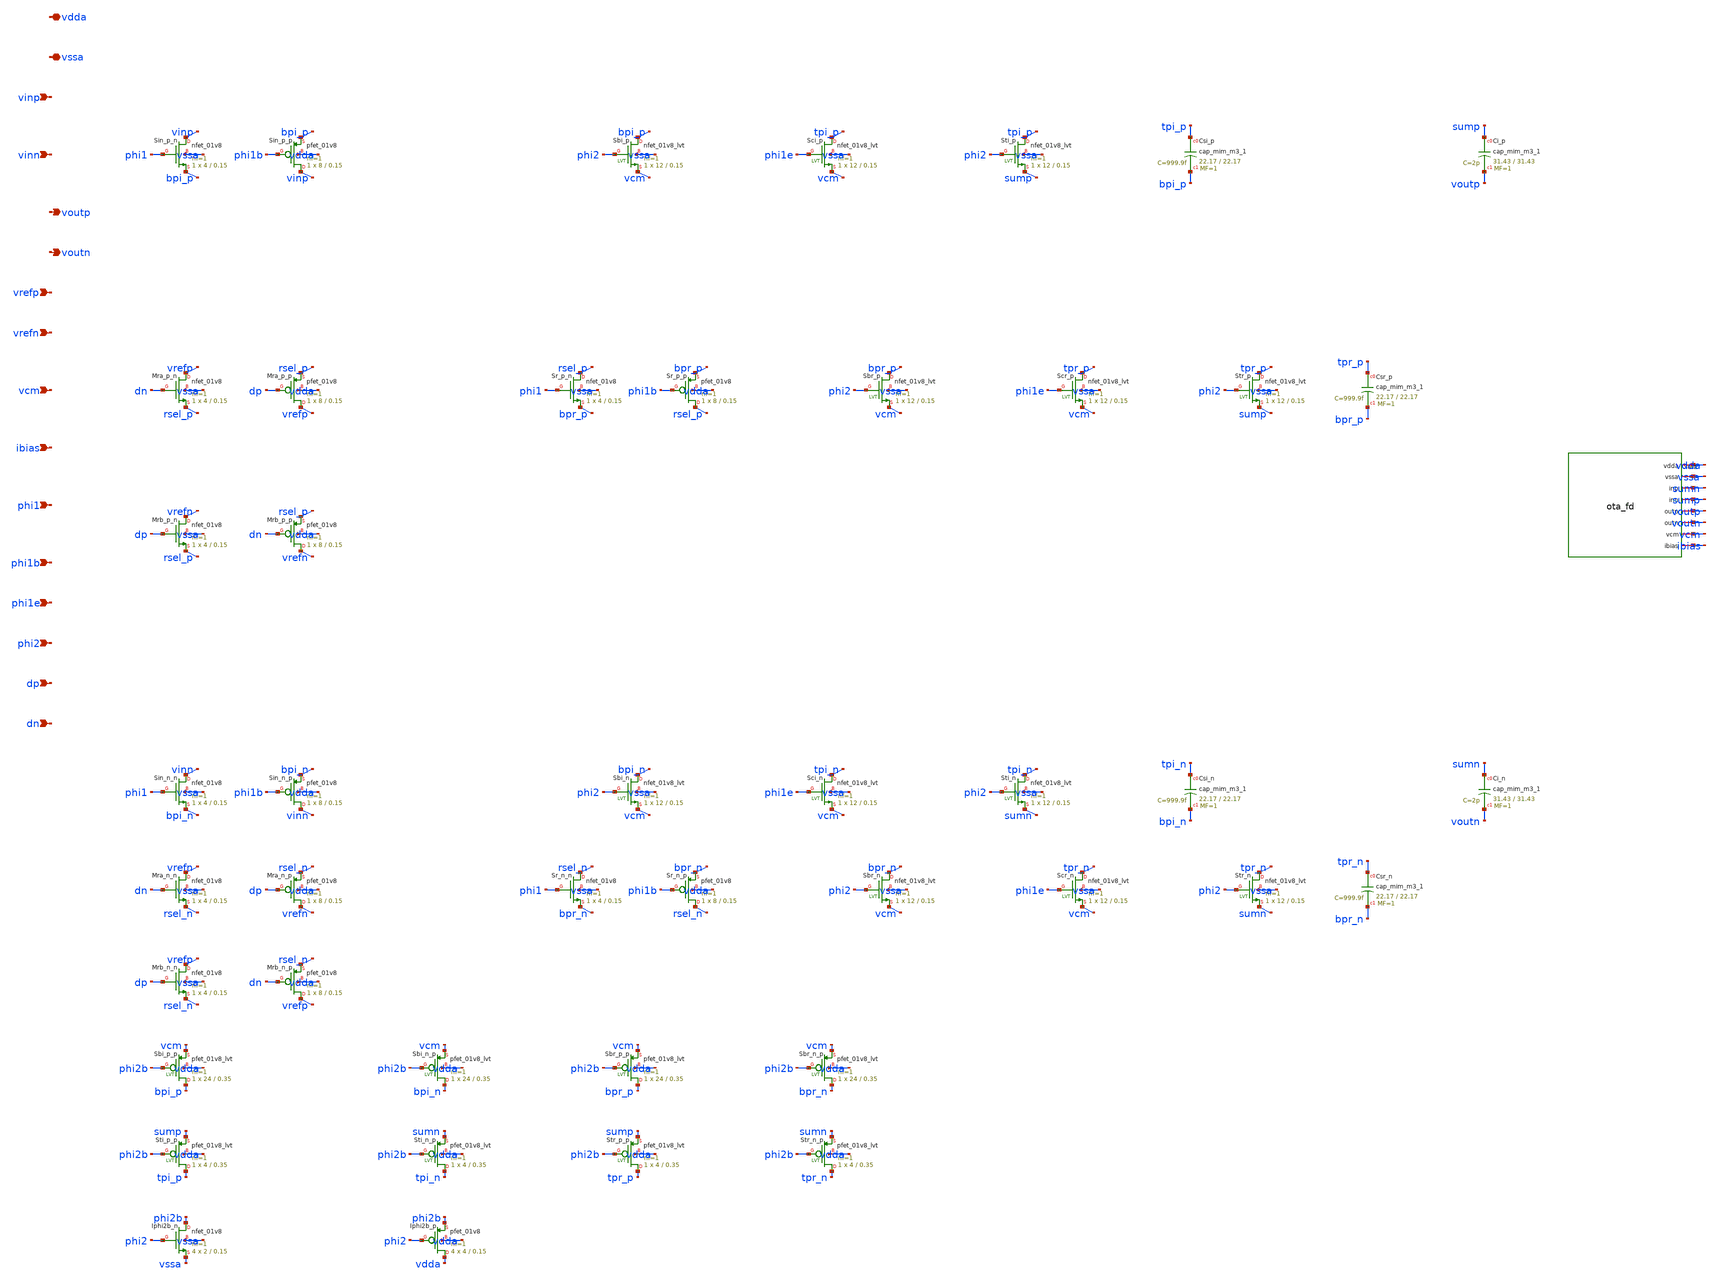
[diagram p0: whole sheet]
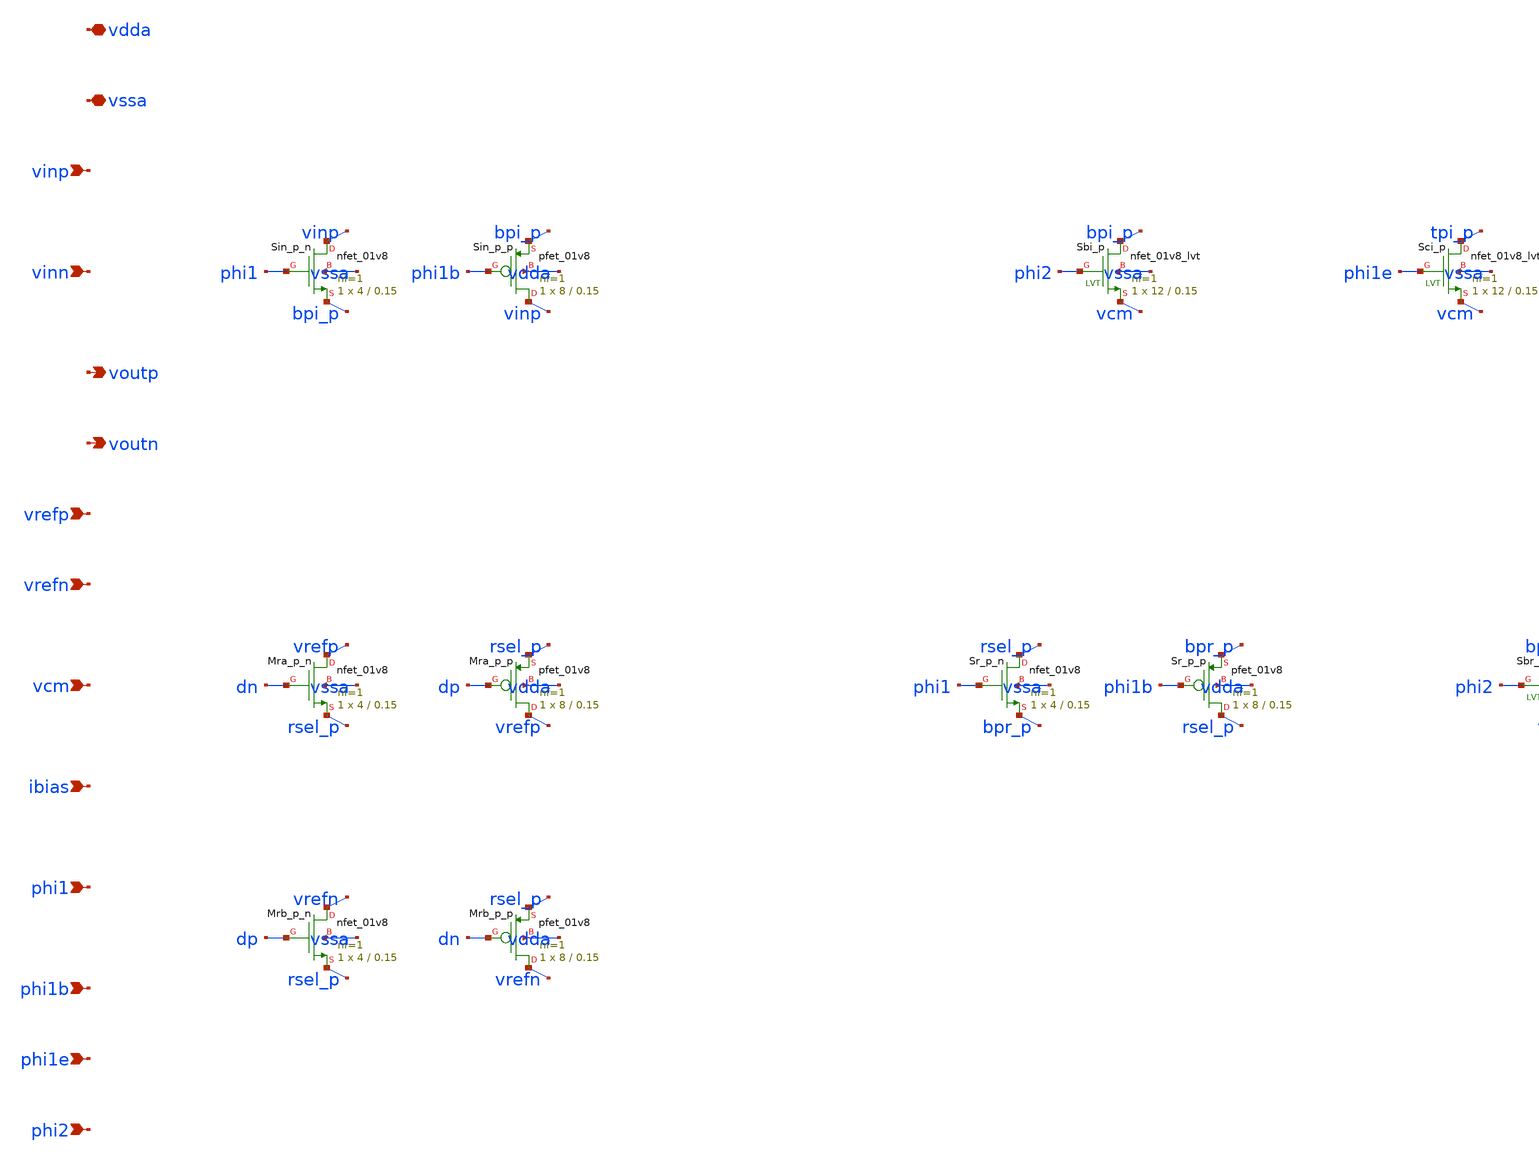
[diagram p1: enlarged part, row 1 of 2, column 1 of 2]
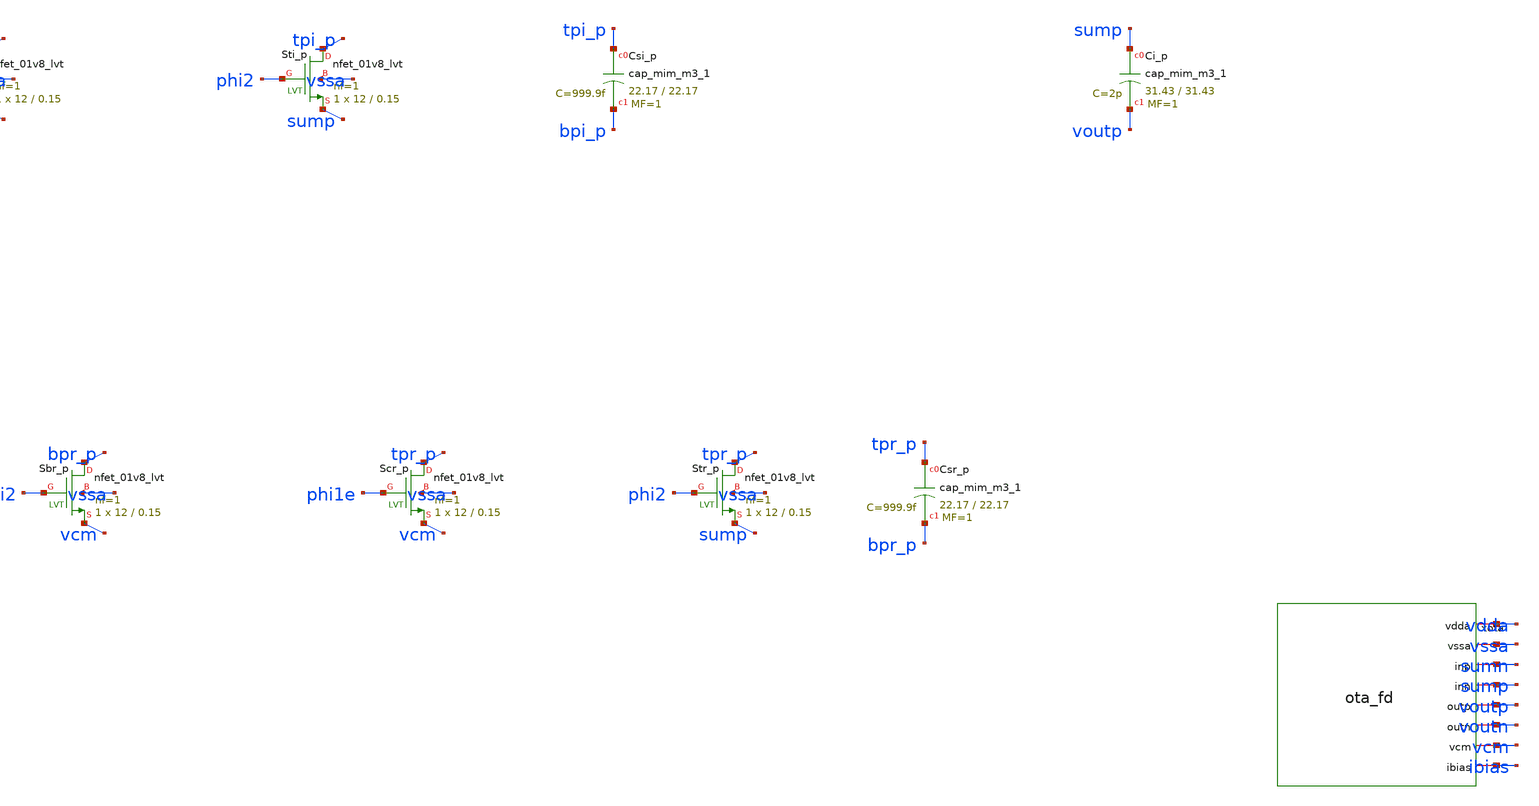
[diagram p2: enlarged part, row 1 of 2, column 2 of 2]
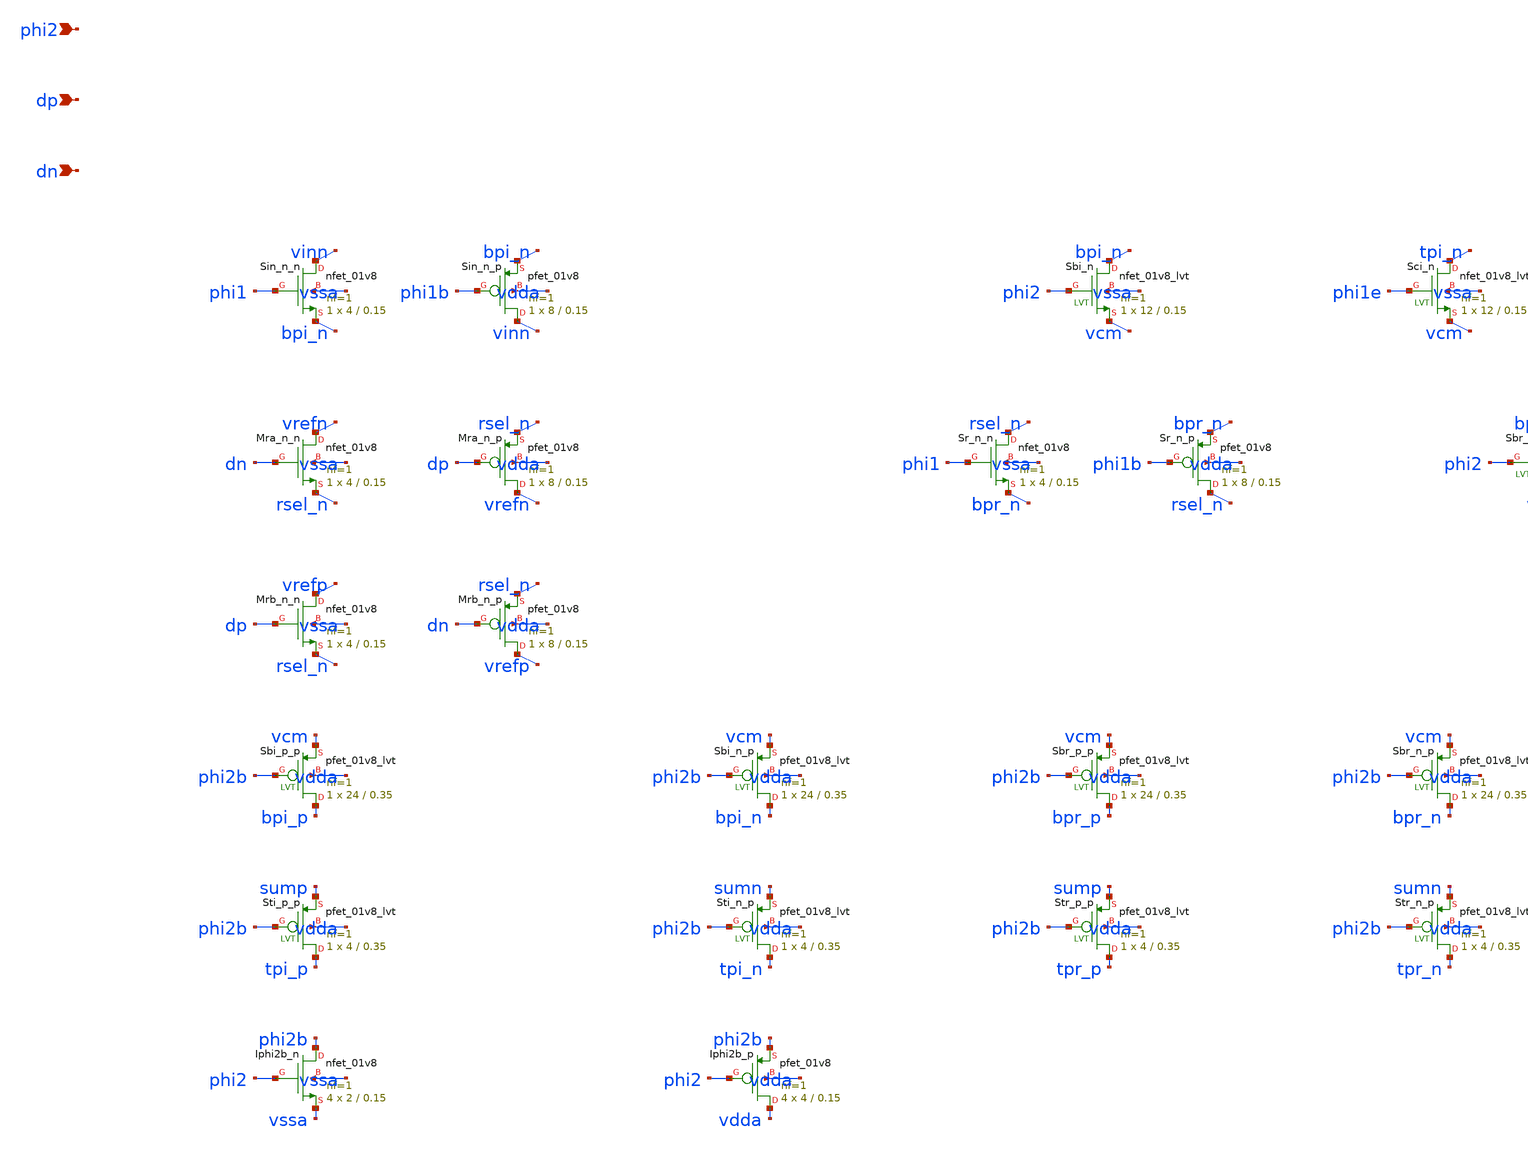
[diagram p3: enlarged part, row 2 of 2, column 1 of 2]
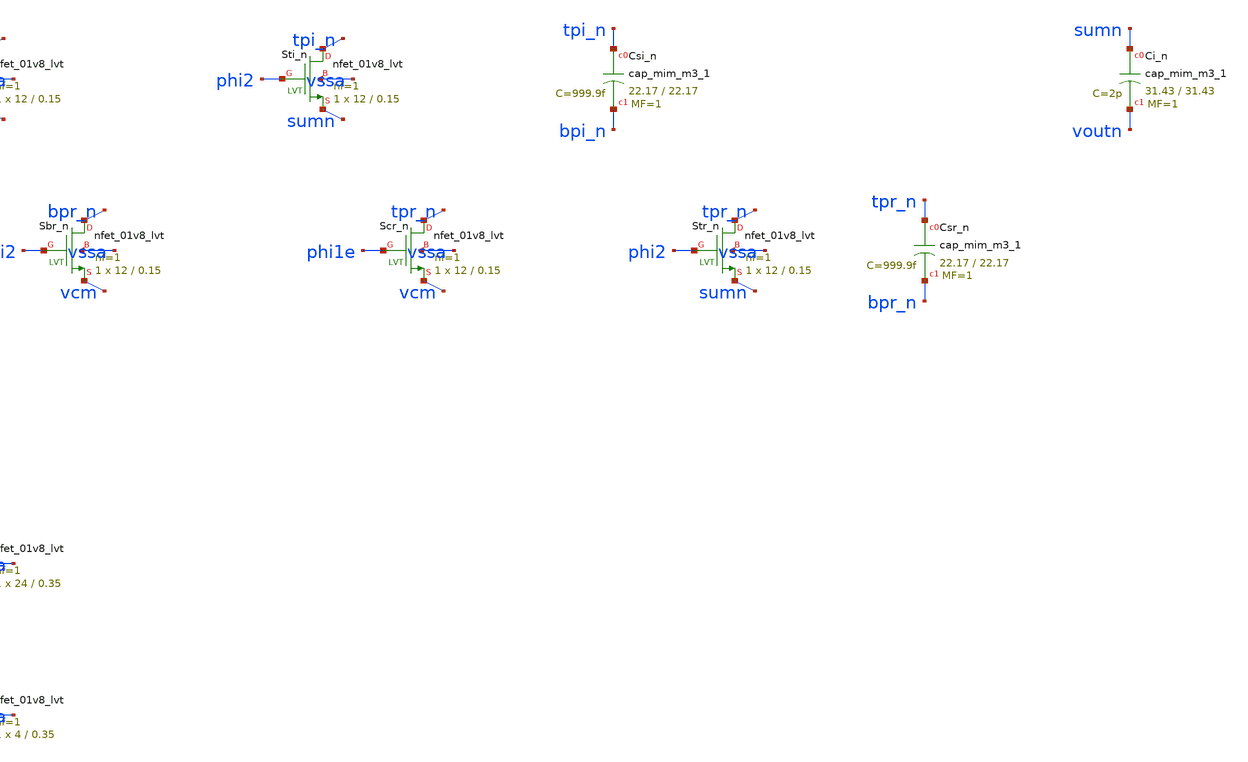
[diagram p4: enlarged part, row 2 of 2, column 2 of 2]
** sch_path: design/integrator/integrator.sch
**.subckt integrator vdda vssa vinp vinn voutp voutn vrefp vrefn vcm ibias phi1 phi1b phi1e phi2 dp
*+ dn
*.iopin vdda
*.iopin vssa
*.ipin vinp
*.ipin vinn
*.opin voutp
*.opin voutn
*.ipin vrefp
*.ipin vrefn
*.ipin vcm
*.ipin ibias
*.ipin phi1
*.ipin phi1b
*.ipin phi1e
*.ipin phi2
*.ipin dp
*.ipin dn
XSin_p_n vinp phi1 bpi_p vssa sky130_fd_pr__nfet_01v8 L=0.15 W=4 nf=1 ad=1.16 as=1.16 pd=8.58
+ ps=8.58 nrd=0.0725 nrs=0.0725 sa=0 sb=0 sd=0 mult=1 m=1
XSin_p_p vinp phi1b bpi_p vdda sky130_fd_pr__pfet_01v8 L=0.15 W=8 nf=1 ad=2.32 as=2.32 pd=16.58
+ ps=16.58 nrd=0.03625 nrs=0.03625 sa=0 sb=0 sd=0 mult=1 m=1
XSbi_p bpi_p phi2 vcm vssa sky130_fd_pr__nfet_01v8_lvt L=0.15 W=12 nf=1 ad=3.48 as=3.48 pd=24.58
+ ps=24.58 nrd=0.02416667 nrs=0.02416667 sa=0 sb=0 sd=0 mult=1 m=1
XSci_p tpi_p phi1e vcm vssa sky130_fd_pr__nfet_01v8_lvt L=0.15 W=12 nf=1 ad=3.48 as=3.48 pd=24.58
+ ps=24.58 nrd=0.02416667 nrs=0.02416667 sa=0 sb=0 sd=0 mult=1 m=1
XSti_p tpi_p phi2 sump vssa sky130_fd_pr__nfet_01v8_lvt L=0.15 W=12 nf=1 ad=3.48 as=3.48 pd=24.58
+ ps=24.58 nrd=0.02416667 nrs=0.02416667 sa=0 sb=0 sd=0 mult=1 m=1
XCsi_p tpi_p bpi_p sky130_fd_pr__cap_mim_m3_1 W=22.17 L=22.17 MF=1 m=1
XMra_p_n vrefp dn rsel_p vssa sky130_fd_pr__nfet_01v8 L=0.15 W=4 nf=1 ad=1.16 as=1.16 pd=8.58
+ ps=8.58 nrd=0.0725 nrs=0.0725 sa=0 sb=0 sd=0 mult=1 m=1
XMra_p_p vrefp dp rsel_p vdda sky130_fd_pr__pfet_01v8 L=0.15 W=8 nf=1 ad=2.32 as=2.32 pd=16.58
+ ps=16.58 nrd=0.03625 nrs=0.03625 sa=0 sb=0 sd=0 mult=1 m=1
XMrb_p_n vrefn dp rsel_p vssa sky130_fd_pr__nfet_01v8 L=0.15 W=4 nf=1 ad=1.16 as=1.16 pd=8.58
+ ps=8.58 nrd=0.0725 nrs=0.0725 sa=0 sb=0 sd=0 mult=1 m=1
XMrb_p_p vrefn dn rsel_p vdda sky130_fd_pr__pfet_01v8 L=0.15 W=8 nf=1 ad=2.32 as=2.32 pd=16.58
+ ps=16.58 nrd=0.03625 nrs=0.03625 sa=0 sb=0 sd=0 mult=1 m=1
XSr_p_n rsel_p phi1 bpr_p vssa sky130_fd_pr__nfet_01v8 L=0.15 W=4 nf=1 ad=1.16 as=1.16 pd=8.58
+ ps=8.58 nrd=0.0725 nrs=0.0725 sa=0 sb=0 sd=0 mult=1 m=1
XSr_p_p rsel_p phi1b bpr_p vdda sky130_fd_pr__pfet_01v8 L=0.15 W=8 nf=1 ad=2.32 as=2.32 pd=16.58
+ ps=16.58 nrd=0.03625 nrs=0.03625 sa=0 sb=0 sd=0 mult=1 m=1
XSbr_p bpr_p phi2 vcm vssa sky130_fd_pr__nfet_01v8_lvt L=0.15 W=12 nf=1 ad=3.48 as=3.48 pd=24.58
+ ps=24.58 nrd=0.02416667 nrs=0.02416667 sa=0 sb=0 sd=0 mult=1 m=1
XScr_p tpr_p phi1e vcm vssa sky130_fd_pr__nfet_01v8_lvt L=0.15 W=12 nf=1 ad=3.48 as=3.48 pd=24.58
+ ps=24.58 nrd=0.02416667 nrs=0.02416667 sa=0 sb=0 sd=0 mult=1 m=1
XStr_p tpr_p phi2 sump vssa sky130_fd_pr__nfet_01v8_lvt L=0.15 W=12 nf=1 ad=3.48 as=3.48 pd=24.58
+ ps=24.58 nrd=0.02416667 nrs=0.02416667 sa=0 sb=0 sd=0 mult=1 m=1
XCsr_p tpr_p bpr_p sky130_fd_pr__cap_mim_m3_1 W=22.17 L=22.17 MF=1 m=1
XCi_p sump voutp sky130_fd_pr__cap_mim_m3_1 W=31.43 L=31.43 MF=1 m=1
XSin_n_n vinn phi1 bpi_n vssa sky130_fd_pr__nfet_01v8 L=0.15 W=4 nf=1 ad=1.16 as=1.16 pd=8.58
+ ps=8.58 nrd=0.0725 nrs=0.0725 sa=0 sb=0 sd=0 mult=1 m=1
XSin_n_p vinn phi1b bpi_n vdda sky130_fd_pr__pfet_01v8 L=0.15 W=8 nf=1 ad=2.32 as=2.32 pd=16.58
+ ps=16.58 nrd=0.03625 nrs=0.03625 sa=0 sb=0 sd=0 mult=1 m=1
XSbi_n bpi_n phi2 vcm vssa sky130_fd_pr__nfet_01v8_lvt L=0.15 W=12 nf=1 ad=3.48 as=3.48 pd=24.58
+ ps=24.58 nrd=0.02416667 nrs=0.02416667 sa=0 sb=0 sd=0 mult=1 m=1
XSci_n tpi_n phi1e vcm vssa sky130_fd_pr__nfet_01v8_lvt L=0.15 W=12 nf=1 ad=3.48 as=3.48 pd=24.58
+ ps=24.58 nrd=0.02416667 nrs=0.02416667 sa=0 sb=0 sd=0 mult=1 m=1
XSti_n tpi_n phi2 sumn vssa sky130_fd_pr__nfet_01v8_lvt L=0.15 W=12 nf=1 ad=3.48 as=3.48 pd=24.58
+ ps=24.58 nrd=0.02416667 nrs=0.02416667 sa=0 sb=0 sd=0 mult=1 m=1
XCsi_n tpi_n bpi_n sky130_fd_pr__cap_mim_m3_1 W=22.17 L=22.17 MF=1 m=1
XMra_n_n vrefn dn rsel_n vssa sky130_fd_pr__nfet_01v8 L=0.15 W=4 nf=1 ad=1.16 as=1.16 pd=8.58
+ ps=8.58 nrd=0.0725 nrs=0.0725 sa=0 sb=0 sd=0 mult=1 m=1
XMra_n_p vrefn dp rsel_n vdda sky130_fd_pr__pfet_01v8 L=0.15 W=8 nf=1 ad=2.32 as=2.32 pd=16.58
+ ps=16.58 nrd=0.03625 nrs=0.03625 sa=0 sb=0 sd=0 mult=1 m=1
XMrb_n_n vrefp dp rsel_n vssa sky130_fd_pr__nfet_01v8 L=0.15 W=4 nf=1 ad=1.16 as=1.16 pd=8.58
+ ps=8.58 nrd=0.0725 nrs=0.0725 sa=0 sb=0 sd=0 mult=1 m=1
XMrb_n_p vrefp dn rsel_n vdda sky130_fd_pr__pfet_01v8 L=0.15 W=8 nf=1 ad=2.32 as=2.32 pd=16.58
+ ps=16.58 nrd=0.03625 nrs=0.03625 sa=0 sb=0 sd=0 mult=1 m=1
XSr_n_n rsel_n phi1 bpr_n vssa sky130_fd_pr__nfet_01v8 L=0.15 W=4 nf=1 ad=1.16 as=1.16 pd=8.58
+ ps=8.58 nrd=0.0725 nrs=0.0725 sa=0 sb=0 sd=0 mult=1 m=1
XSr_n_p rsel_n phi1b bpr_n vdda sky130_fd_pr__pfet_01v8 L=0.15 W=8 nf=1 ad=2.32 as=2.32 pd=16.58
+ ps=16.58 nrd=0.03625 nrs=0.03625 sa=0 sb=0 sd=0 mult=1 m=1
XSbr_n bpr_n phi2 vcm vssa sky130_fd_pr__nfet_01v8_lvt L=0.15 W=12 nf=1 ad=3.48 as=3.48 pd=24.58
+ ps=24.58 nrd=0.02416667 nrs=0.02416667 sa=0 sb=0 sd=0 mult=1 m=1
XScr_n tpr_n phi1e vcm vssa sky130_fd_pr__nfet_01v8_lvt L=0.15 W=12 nf=1 ad=3.48 as=3.48 pd=24.58
+ ps=24.58 nrd=0.02416667 nrs=0.02416667 sa=0 sb=0 sd=0 mult=1 m=1
XStr_n tpr_n phi2 sumn vssa sky130_fd_pr__nfet_01v8_lvt L=0.15 W=12 nf=1 ad=3.48 as=3.48 pd=24.58
+ ps=24.58 nrd=0.02416667 nrs=0.02416667 sa=0 sb=0 sd=0 mult=1 m=1
XCsr_n tpr_n bpr_n sky130_fd_pr__cap_mim_m3_1 W=22.17 L=22.17 MF=1 m=1
XCi_n sumn voutn sky130_fd_pr__cap_mim_m3_1 W=31.43 L=31.43 MF=1 m=1
xota vdda vssa sumn sump voutp voutn vcm ibias ota_fd
XSbi_p_p bpi_p phi2b vcm vdda sky130_fd_pr__pfet_01v8_lvt L=0.35 W=24 nf=1 ad=6.96 as=6.96 pd=48.58
+ ps=48.58 nrd=0.012083333 nrs=0.012083333 sa=0 sb=0 sd=0 mult=1 m=1
XSbi_n_p bpi_n phi2b vcm vdda sky130_fd_pr__pfet_01v8_lvt L=0.35 W=24 nf=1 ad=6.96 as=6.96 pd=48.58
+ ps=48.58 nrd=0.012083333 nrs=0.012083333 sa=0 sb=0 sd=0 mult=1 m=1
XSbr_p_p bpr_p phi2b vcm vdda sky130_fd_pr__pfet_01v8_lvt L=0.35 W=24 nf=1 ad=6.96 as=6.96 pd=48.58
+ ps=48.58 nrd=0.012083333 nrs=0.012083333 sa=0 sb=0 sd=0 mult=1 m=1
XSbr_n_p bpr_n phi2b vcm vdda sky130_fd_pr__pfet_01v8_lvt L=0.35 W=24 nf=1 ad=6.96 as=6.96 pd=48.58
+ ps=48.58 nrd=0.012083333 nrs=0.012083333 sa=0 sb=0 sd=0 mult=1 m=1
XSti_p_p tpi_p phi2b sump vdda sky130_fd_pr__pfet_01v8_lvt L=0.35 W=4 nf=1 ad=1.16 as=1.16 pd=8.58
+ ps=8.58 nrd=0.0725 nrs=0.0725 sa=0 sb=0 sd=0 mult=1 m=1
XSti_n_p tpi_n phi2b sumn vdda sky130_fd_pr__pfet_01v8_lvt L=0.35 W=4 nf=1 ad=1.16 as=1.16 pd=8.58
+ ps=8.58 nrd=0.0725 nrs=0.0725 sa=0 sb=0 sd=0 mult=1 m=1
XStr_p_p tpr_p phi2b sump vdda sky130_fd_pr__pfet_01v8_lvt L=0.35 W=4 nf=1 ad=1.16 as=1.16 pd=8.58
+ ps=8.58 nrd=0.0725 nrs=0.0725 sa=0 sb=0 sd=0 mult=1 m=1
XStr_n_p tpr_n phi2b sumn vdda sky130_fd_pr__pfet_01v8_lvt L=0.35 W=4 nf=1 ad=1.16 as=1.16 pd=8.58
+ ps=8.58 nrd=0.0725 nrs=0.0725 sa=0 sb=0 sd=0 mult=1 m=1
XIphi2b_n phi2b phi2 vssa vssa sky130_fd_pr__nfet_01v8 L=0.15 W=2 nf=1 ad=0.58 as=0.58 pd=4.58
+ ps=4.58 nrd=0.145 nrs=0.145 sa=0 sb=0 sd=0 mult=4 m=4
XIphi2b_p vdda phi2 phi2b vdda sky130_fd_pr__pfet_01v8 L=0.15 W=4 nf=1 ad=1.16 as=1.16 pd=8.58
+ ps=8.58 nrd=0.0725 nrs=0.0725 sa=0 sb=0 sd=0 mult=4 m=4
**.ends

* expanding   symbol:  ota/ota_fd.sym # of pins=8
** sym_path: design/ota/ota_fd.sym
** sch_path: design/ota/ota_fd.sch
.subckt ota_fd vdda vssa inp inn outp outn vcm ibias
*.iopin vdda
*.iopin vssa
*.ipin inp
*.ipin inn
*.opin outp
*.opin outn
*.ipin vcm
*.ipin ibias
XM1 fa inp tail vssa sky130_fd_pr__nfet_01v8 L=0.5 W=16.0 nf=1 ad='int((1 + 1)/2) * 16.0 / 1 * 0.29'
+ as='int((1 + 2)/2) * 16.0 / 1 * 0.29' pd='2*int((1 + 1)/2) * (16.0 / 1 + 0.29)' ps='2*int((1 + 2)/2) * (16.0 / 1 + 0.29)'
+ nrd='0.29 / 16.0 ' nrs='0.29 / 16.0 ' sa=0 sb=0 sd=0 mult=1 m=1
XM2 fb inn tail vssa sky130_fd_pr__nfet_01v8 L=0.5 W=16.0 nf=1 ad='int((1 + 1)/2) * 16.0 / 1 * 0.29'
+ as='int((1 + 2)/2) * 16.0 / 1 * 0.29' pd='2*int((1 + 1)/2) * (16.0 / 1 + 0.29)' ps='2*int((1 + 2)/2) * (16.0 / 1 + 0.29)'
+ nrd='0.29 / 16.0 ' nrs='0.29 / 16.0 ' sa=0 sb=0 sd=0 mult=1 m=1
XMT tail ibias vssa vssa sky130_fd_pr__nfet_01v8 L=0.5 W=2.0 nf=1 ad='int((1 + 1)/2) * 2.0 / 1 * 0.29'
+ as='int((1 + 2)/2) * 2.0 / 1 * 0.29' pd='2*int((1 + 1)/2) * (2.0 / 1 + 0.29)' ps='2*int((1 + 2)/2) * (2.0 / 1 + 0.29)'
+ nrd='0.29 / 2.0 ' nrs='0.29 / 2.0 ' sa=0 sb=0 sd=0 mult=16 m=16
XMP1 fa cr vdda vdda sky130_fd_pr__pfet_01v8 L=0.5 W=10.0 nf=1 ad='int((nf+1)/2) * W/nf * 0.29' as='int((nf+2)/2) * W/nf * 0.29'
+ pd='2*int((nf+1)/2) * (W/nf + 0.29)' ps='2*int((nf+2)/2) * (W/nf + 0.29)' nrd='0.29 / W' nrs='0.29 / W'
+ sa=0 sb=0 sd=0 mult=8 m=8
XMP2 fb cr vdda vdda sky130_fd_pr__pfet_01v8 L=0.5 W=10.0 nf=1 ad='int((nf+1)/2) * W/nf * 0.29' as='int((nf+2)/2) * W/nf * 0.29'
+ pd='2*int((nf+1)/2) * (W/nf + 0.29)' ps='2*int((nf+2)/2) * (W/nf + 0.29)' nrd='0.29 / W' nrs='0.29 / W'
+ sa=0 sb=0 sd=0 mult=8 m=8
XMPC1 outn vcp fa vdda sky130_fd_pr__pfet_01v8 L=0.5 W=10.0 nf=1 ad='int((nf+1)/2) * W/nf * 0.29' as='int((nf+2)/2) * W/nf * 0.29'
+ pd='2*int((nf+1)/2) * (W/nf + 0.29)' ps='2*int((nf+2)/2) * (W/nf + 0.29)' nrd='0.29 / W' nrs='0.29 / W'
+ sa=0 sb=0 sd=0 mult=4 m=4
XMPC2 outp vcp fb vdda sky130_fd_pr__pfet_01v8 L=0.5 W=10.0 nf=1 ad='int((nf+1)/2) * W/nf * 0.29' as='int((nf+2)/2) * W/nf * 0.29'
+ pd='2*int((nf+1)/2) * (W/nf + 0.29)' ps='2*int((nf+2)/2) * (W/nf + 0.29)' nrd='0.29 / W' nrs='0.29 / W'
+ sa=0 sb=0 sd=0 mult=4 m=4
XMNC1 outn vcn sa vssa sky130_fd_pr__nfet_01v8 L=0.5 W=7.0 nf=1 ad='int((1 + 1)/2) * 7.0 / 1 * 0.29'
+ as='int((1 + 2)/2) * 7.0 / 1 * 0.29' pd='2*int((1 + 1)/2) * (7.0 / 1 + 0.29)' ps='2*int((1 + 2)/2) * (7.0 / 1 + 0.29)'
+ nrd='0.29 / 7.0 ' nrs='0.29 / 7.0 ' sa=0 sb=0 sd=0 mult=2 m=2
XMNC2 outp vcn sb vssa sky130_fd_pr__nfet_01v8 L=0.5 W=7.0 nf=1 ad='int((1 + 1)/2) * 7.0 / 1 * 0.29'
+ as='int((1 + 2)/2) * 7.0 / 1 * 0.29' pd='2*int((1 + 1)/2) * (7.0 / 1 + 0.29)' ps='2*int((1 + 2)/2) * (7.0 / 1 + 0.29)'
+ nrd='0.29 / 7.0 ' nrs='0.29 / 7.0 ' sa=0 sb=0 sd=0 mult=2 m=2
XMN1 sa ibias vssa vssa sky130_fd_pr__nfet_01v8 L=0.5 W=2.0 nf=1 ad='int((1 + 1)/2) * 2.0 / 1 * 0.29'
+ as='int((1 + 2)/2) * 2.0 / 1 * 0.29' pd='2*int((1 + 1)/2) * (2.0 / 1 + 0.29)' ps='2*int((1 + 2)/2) * (2.0 / 1 + 0.29)'
+ nrd='0.29 / 2.0 ' nrs='0.29 / 2.0 ' sa=0 sb=0 sd=0 mult=8 m=8
XMN2 sb ibias vssa vssa sky130_fd_pr__nfet_01v8 L=0.5 W=2.0 nf=1 ad='int((1 + 1)/2) * 2.0 / 1 * 0.29'
+ as='int((1 + 2)/2) * 2.0 / 1 * 0.29' pd='2*int((1 + 1)/2) * (2.0 / 1 + 0.29)' ps='2*int((1 + 2)/2) * (2.0 / 1 + 0.29)'
+ nrd='0.29 / 2.0 ' nrs='0.29 / 2.0 ' sa=0 sb=0 sd=0 mult=8 m=8
XMB1 ibias ibias vssa vssa sky130_fd_pr__nfet_01v8 L=0.5 W=2.0 nf=1 ad='int((1 + 1)/2) * 2.0 / 1 * 0.29'
+ as='int((1 + 2)/2) * 2.0 / 1 * 0.29' pd='2*int((1 + 1)/2) * (2.0 / 1 + 0.29)' ps='2*int((1 + 2)/2) * (2.0 / 1 + 0.29)'
+ nrd='0.29 / 2.0 ' nrs='0.29 / 2.0 ' sa=0 sb=0 sd=0 mult=1 m=1
XMBP1 vbpd vbpd vdda vdda sky130_fd_pr__pfet_01v8 L=0.5 W=5.0 nf=1 ad='int((nf+1)/2) * W/nf * 0.29' as='int((nf+2)/2) * W/nf * 0.29'
+ pd='2*int((nf+1)/2) * (W/nf + 0.29)' ps='2*int((nf+2)/2) * (W/nf + 0.29)' nrd='0.29 / W' nrs='0.29 / W'
+ sa=0 sb=0 sd=0 mult=1 m=1
XMBN1 vbpd ibias vssa vssa sky130_fd_pr__nfet_01v8 L=0.5 W=2.0 nf=1 ad='int((1 + 1)/2) * 2.0 / 1 * 0.29'
+ as='int((1 + 2)/2) * 2.0 / 1 * 0.29' pd='2*int((1 + 1)/2) * (2.0 / 1 + 0.29)' ps='2*int((1 + 2)/2) * (2.0 / 1 + 0.29)'
+ nrd='0.29 / 2.0 ' nrs='0.29 / 2.0 ' sa=0 sb=0 sd=0 mult=1 m=1
XMBP2 vcn vbpd vdda vdda sky130_fd_pr__pfet_01v8 L=0.5 W=5.0 nf=1 ad='int((nf+1)/2) * W/nf * 0.29' as='int((nf+2)/2) * W/nf * 0.29'
+ pd='2*int((nf+1)/2) * (W/nf + 0.29)' ps='2*int((nf+2)/2) * (W/nf + 0.29)' nrd='0.29 / W' nrs='0.29 / W'
+ sa=0 sb=0 sd=0 mult=1 m=1
XMBCN vcn vcn vssa vssa sky130_fd_pr__nfet_01v8 L=1.0 W=0.42 nf=1 ad='int((1 + 1)/2) * 0.42 / 1 * 0.29'
+ as='int((1 + 2)/2) * 0.42 / 1 * 0.29' pd='2*int((1 + 1)/2) * (0.42 / 1 + 0.29)' ps='2*int((1 + 2)/2) * (0.42 / 1 + 0.29)'
+ nrd='0.29 / 0.42 ' nrs='0.29 / 0.42 ' sa=0 sb=0 sd=0 mult=1 m=1
XMBCP vcp vcp vdda vdda sky130_fd_pr__pfet_01v8 L=0.6 W=0.42 nf=1 ad='int((nf+1)/2) * W/nf * 0.29' as='int((nf+2)/2) * W/nf * 0.29'
+ pd='2*int((nf+1)/2) * (W/nf + 0.29)' ps='2*int((nf+2)/2) * (W/nf + 0.29)' nrd='0.29 / W' nrs='0.29 / W'
+ sa=0 sb=0 sd=0 mult=1 m=1
XMBN2 vcp ibias vssa vssa sky130_fd_pr__nfet_01v8 L=0.5 W=2.0 nf=1 ad='int((1 + 1)/2) * 2.0 / 1 * 0.29'
+ as='int((1 + 2)/2) * 2.0 / 1 * 0.29' pd='2*int((1 + 1)/2) * (2.0 / 1 + 0.29)' ps='2*int((1 + 2)/2) * (2.0 / 1 + 0.29)'
+ nrd='0.29 / 2.0 ' nrs='0.29 / 2.0 ' sa=0 sb=0 sd=0 mult=1 m=1
XMCS cs cmx ct vssa sky130_fd_pr__nfet_01v8 L=0.5 W=2.0 nf=1 ad='int((1 + 1)/2) * 2.0 / 1 * 0.29' as='int((1 + 2)/2) * 2.0 / 1 * 0.29'
+ pd='2*int((1 + 1)/2) * (2.0 / 1 + 0.29)' ps='2*int((1 + 2)/2) * (2.0 / 1 + 0.29)' nrd='0.29 / 2.0 ' nrs='0.29 / 2.0 '
+ sa=0 sb=0 sd=0 mult=2 m=2
XRcm1 cmx outp vssa sky130_fd_pr__res_xhigh_po_0p35 L=350 mult=1 m=1
XRcm2 cmx outn vssa sky130_fd_pr__res_xhigh_po_0p35 L=350 mult=1 m=1
XCff1 outp cmx sky130_fd_pr__cap_mim_m3_1 W=7.07 L=7.07 MF=1 m=1
XCff2 outn cmx sky130_fd_pr__cap_mim_m3_1 W=7.07 L=7.07 MF=1 m=1
XMCR cr vcm ct vssa sky130_fd_pr__nfet_01v8 L=0.5 W=2.0 nf=1 ad='int((1 + 1)/2) * 2.0 / 1 * 0.29' as='int((1 + 2)/2) * 2.0 / 1 * 0.29'
+ pd='2*int((1 + 1)/2) * (2.0 / 1 + 0.29)' ps='2*int((1 + 2)/2) * (2.0 / 1 + 0.29)' nrd='0.29 / 2.0 ' nrs='0.29 / 2.0 '
+ sa=0 sb=0 sd=0 mult=2 m=2
XMCT ct ibias vssa vssa sky130_fd_pr__nfet_01v8 L=0.5 W=2.0 nf=1 ad='int((1 + 1)/2) * 2.0 / 1 * 0.29'
+ as='int((1 + 2)/2) * 2.0 / 1 * 0.29' pd='2*int((1 + 1)/2) * (2.0 / 1 + 0.29)' ps='2*int((1 + 2)/2) * (2.0 / 1 + 0.29)'
+ nrd='0.29 / 2.0 ' nrs='0.29 / 2.0 ' sa=0 sb=0 sd=0 mult=2 m=2
XMCPS cs cs vdda vdda sky130_fd_pr__pfet_01v8 L=0.5 W=5.0 nf=1 ad='int((nf+1)/2) * W/nf * 0.29' as='int((nf+2)/2) * W/nf * 0.29'
+ pd='2*int((nf+1)/2) * (W/nf + 0.29)' ps='2*int((nf+2)/2) * (W/nf + 0.29)' nrd='0.29 / W' nrs='0.29 / W'
+ sa=0 sb=0 sd=0 mult=1 m=1
XMCPR cr cs vdda vdda sky130_fd_pr__pfet_01v8 L=0.5 W=5.0 nf=1 ad='int((nf+1)/2) * W/nf * 0.29' as='int((nf+2)/2) * W/nf * 0.29'
+ pd='2*int((nf+1)/2) * (W/nf + 0.29)' ps='2*int((nf+2)/2) * (W/nf + 0.29)' nrd='0.29 / W' nrs='0.29 / W'
+ sa=0 sb=0 sd=0 mult=1 m=1
XCcm nz vdda sky130_fd_pr__cap_mim_m3_1 W=44.2 L=44.2 MF=1 m=1
XRz nz cr vssa sky130_fd_pr__res_high_po_0p35 L=4.5 mult=1 m=1
.ends

.end
